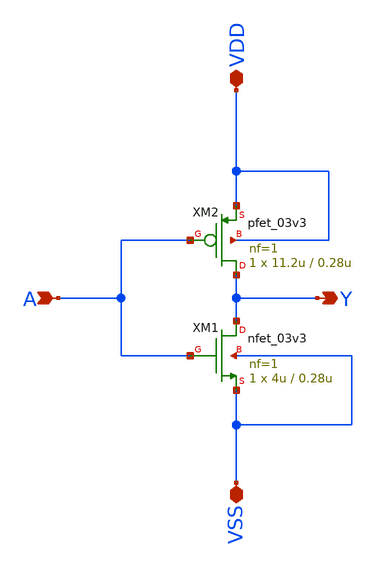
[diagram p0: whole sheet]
** sch_path: xschem/pll_dac/sw_inv7.sch
**.subckt sw_inv7 A VDD VSS Y
*.ipin A
*.iopin VDD
*.iopin VSS
*.opin Y
XM1 Y A VSS VSS nfet_03v3 L=0.28u W=4u nf=1 ad='int((nf+1)/2) * W/nf * 0.18u' as='int((nf+2)/2) * W/nf * 0.18u'
+ pd='2*int((nf+1)/2) * (W/nf + 0.18u)' ps='2*int((nf+2)/2) * (W/nf + 0.18u)' nrd='0.18u / W' nrs='0.18u / W'
+ sa=0 sb=0 sd=0 m=1
XM2 Y A VDD VDD pfet_03v3 L=0.28u W=11.2u nf=1 ad='int((nf+1)/2) * W/nf * 0.18u' as='int((nf+2)/2) * W/nf * 0.18u'
+ pd='2*int((nf+1)/2) * (W/nf + 0.18u)' ps='2*int((nf+2)/2) * (W/nf + 0.18u)' nrd='0.18u / W' nrs='0.18u / W'
+ sa=0 sb=0 sd=0 m=1
**.ends
.end
